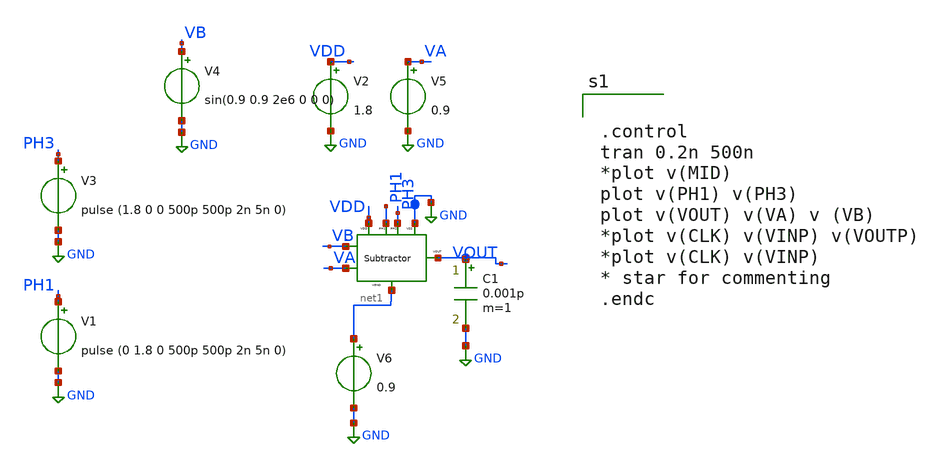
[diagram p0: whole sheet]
** sch_path: xschem/xschem_BGR_Top/Sigma_Delta/Subtractor/Subtractor_TB.sch
**.subckt Subtractor_TB
V1 PH1 GND pulse (0 1.8 0 500p 500p 2n 5n 0)
V2 VDD GND 1.8
X1 net1 PH3 VB VOUT VDD GND PH1 VA Subtractor
V3 PH3 GND pulse (1.8 0 0 500p 500p 2n 5n 0)
V4 VB GND sin(0.9 0.9 2e6 0 0 0)
V6 net1 GND 0.9
V5 VA GND 0.9
C1 VOUT GND 0.001p m=1
**** begin user architecture code


.control
tran 0.2n 500n
*plot v(MID)
plot v(PH1) v(PH3)
plot v(VOUT) v(VA) v (VB)
*plot v(CLK) v(VINP) v(VOUTP)
*plot v(CLK) v(VINP)
* star for commenting
.endc


** opencircuitdesign pdks install
.lib $::SKYWATER_MODELS/sky130.lib.spice tt


**** end user architecture code
**.ends

* expanding   symbol:  Sigma_Delta/Subtractor/Subtractor.sym # of pins=8
** sym_path: xschem/xschem_BGR_Top/Sigma_Delta/Subtractor/Subtractor.sym
** sch_path: xschem/xschem_BGR_Top/Sigma_Delta/Subtractor/Subtractor.sch
.subckt Subtractor VGND PH2 B VOUT VDD VSS PH1 A
*.iopin VDD
*.iopin PH1
*.iopin A
*.iopin VOUT
*.iopin B
*.iopin PH2
*.iopin VGND
*.iopin VSS
XTG3 VSS PH1 VDD B MID TG
XTG4 VSS PH1 VDD VOUT A TG
XM2 MID PH2 VGND VSS sky130_fd_pr__nfet_01v8 L=0.15 W=1.25 nf=1 ad='int((nf+1)/2) * W/nf * 0.29' as='int((nf+2)/2) * W/nf * 0.29'
+ pd='2*int((nf+1)/2) * (W/nf + 0.29)' ps='2*int((nf+2)/2) * (W/nf + 0.29)' nrd='0.29 / W' nrs='0.29 / W'
+ sa=0 sb=0 sd=0 mult=2 m=2
XC1 VOUT MID sky130_fd_pr__cap_mim_m3_1 W=25 L=25 MF=1 m=1
.ends


* expanding   symbol:  Sigma_Delta/Transmission_Gate/TG.sym # of pins=5
** sym_path: xschem/xschem_BGR_Top/Sigma_Delta/Transmission_Gate/TG.sym
** sch_path: xschem/xschem_BGR_Top/Sigma_Delta/Transmission_Gate/TG.sch
.subckt TG VSS CLK VDD A B
*.iopin VDD
*.iopin VSS
*.iopin A
*.iopin B
*.iopin CLK
XM1 A CLK B VSS sky130_fd_pr__nfet_01v8 L=0.15 W=10 nf=1 ad='int((nf+1)/2) * W/nf * 0.29' as='int((nf+2)/2) * W/nf * 0.29'
+ pd='2*int((nf+1)/2) * (W/nf + 0.29)' ps='2*int((nf+2)/2) * (W/nf + 0.29)' nrd='0.29 / W' nrs='0.29 / W'
+ sa=0 sb=0 sd=0 mult=1 m=1
XM2 B CLKB A VDD sky130_fd_pr__pfet_01v8 L=0.15 W=20 nf=2 ad='int((nf+1)/2) * W/nf * 0.29' as='int((nf+2)/2) * W/nf * 0.29'
+ pd='2*int((nf+1)/2) * (W/nf + 0.29)' ps='2*int((nf+2)/2) * (W/nf + 0.29)' nrd='0.29 / W' nrs='0.29 / W'
+ sa=0 sb=0 sd=0 mult=1 m=1
XM3 CLKB CLK VSS VSS sky130_fd_pr__nfet_01v8 L=0.15 W=10 nf=5 ad='int((nf+1)/2) * W/nf * 0.29' as='int((nf+2)/2) * W/nf * 0.29'
+ pd='2*int((nf+1)/2) * (W/nf + 0.29)' ps='2*int((nf+2)/2) * (W/nf + 0.29)' nrd='0.29 / W' nrs='0.29 / W'
+ sa=0 sb=0 sd=0 mult=1 m=1
XM4 CLKB CLK VDD VDD sky130_fd_pr__pfet_01v8 L=0.15 W=20 nf=10 ad='int((nf+1)/2) * W/nf * 0.29' as='int((nf+2)/2) * W/nf * 0.29'
+ pd='2*int((nf+1)/2) * (W/nf + 0.29)' ps='2*int((nf+2)/2) * (W/nf + 0.29)' nrd='0.29 / W' nrs='0.29 / W'
+ sa=0 sb=0 sd=0 mult=1 m=1
.ends

.GLOBAL GND
.end
